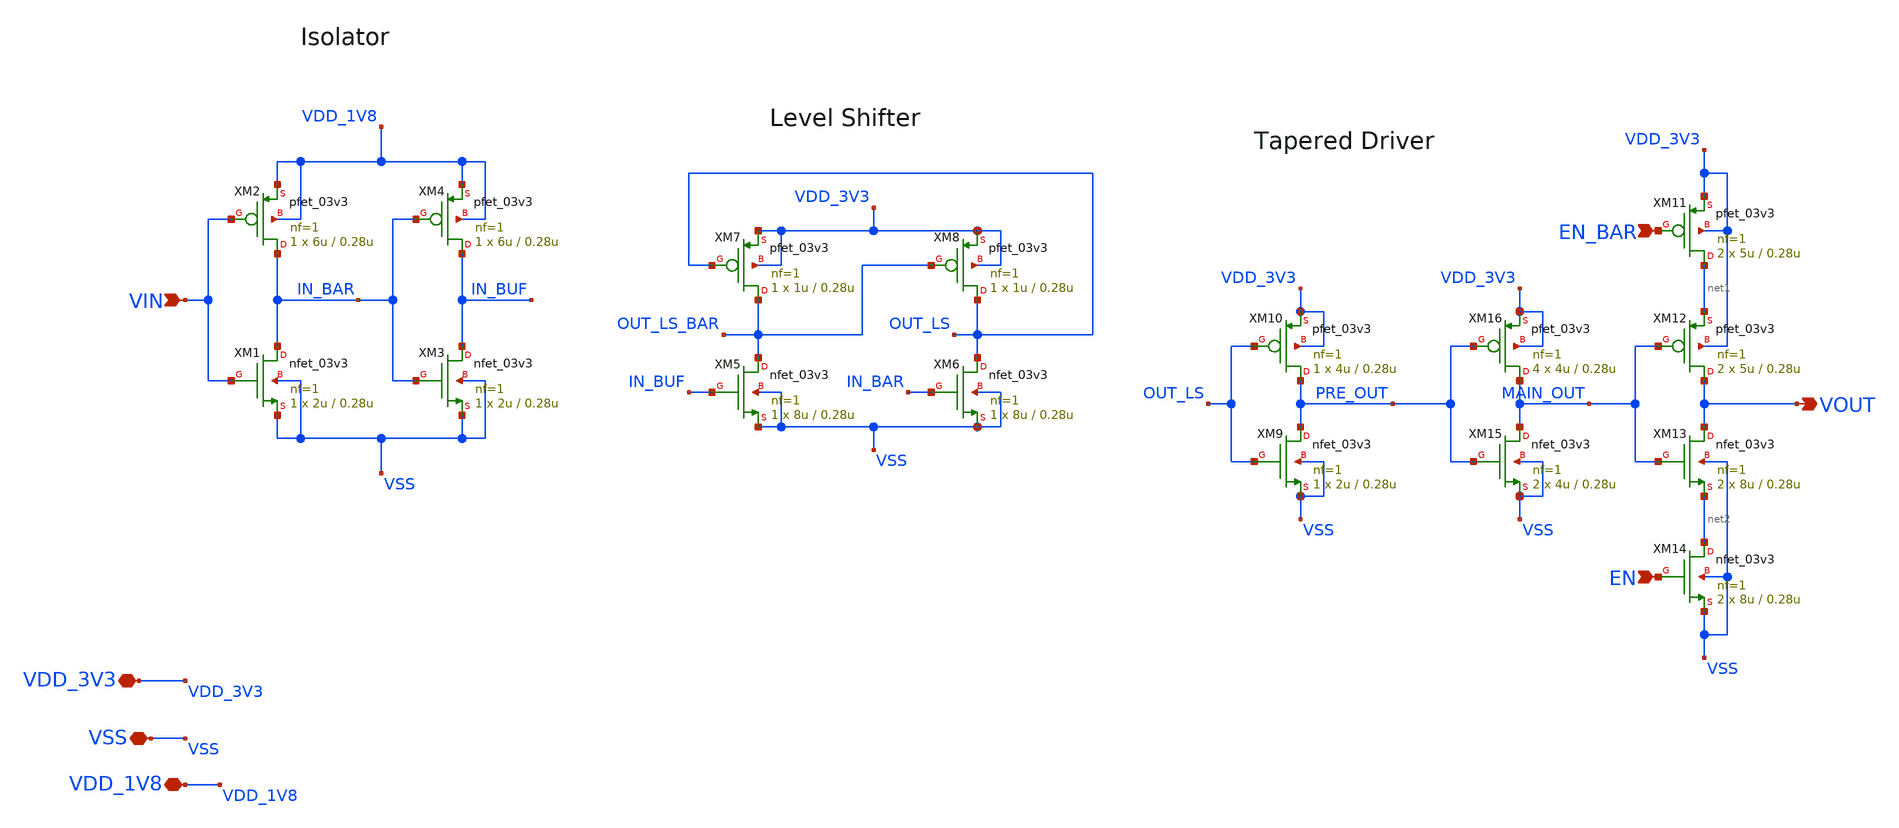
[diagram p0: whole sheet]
** sch_path: src/Output_Buffer/output_buffer.sch
**.subckt output_buffer VIN VSS VDD_1V8 EN EN_BAR VOUT VDD_3V3
*.ipin VIN
*.iopin VSS
*.iopin VDD_1V8
*.ipin EN
*.ipin EN_BAR
*.opin VOUT
*.iopin VDD_3V3
XM1 IN_BAR VIN VSS VSS nfet_03v3 L=0.28u W=2u nf=1 ad='int((nf+1)/2) * W/nf * 0.18u' as='int((nf+2)/2) * W/nf * 0.18u'
+ pd='2*int((nf+1)/2) * (W/nf + 0.18u)' ps='2*int((nf+2)/2) * (W/nf + 0.18u)' nrd='0.18u / W' nrs='0.18u / W'
+ sa=0 sb=0 sd=0 m=1
XM2 IN_BAR VIN VDD_1V8 VDD_1V8 pfet_03v3 L=0.28u W=6u nf=1 ad='int((nf+1)/2) * W/nf * 0.18u' as='int((nf+2)/2) * W/nf * 0.18u'
+ pd='2*int((nf+1)/2) * (W/nf + 0.18u)' ps='2*int((nf+2)/2) * (W/nf + 0.18u)' nrd='0.18u / W' nrs='0.18u / W'
+ sa=0 sb=0 sd=0 m=1
XM3 IN_BUF IN_BAR VSS VSS nfet_03v3 L=0.28u W=2u nf=1 ad='int((nf+1)/2) * W/nf * 0.18u' as='int((nf+2)/2) * W/nf * 0.18u'
+ pd='2*int((nf+1)/2) * (W/nf + 0.18u)' ps='2*int((nf+2)/2) * (W/nf + 0.18u)' nrd='0.18u / W' nrs='0.18u / W'
+ sa=0 sb=0 sd=0 m=1
XM4 IN_BUF IN_BAR VDD_1V8 VDD_1V8 pfet_03v3 L=0.28u W=6u nf=1 ad='int((nf+1)/2) * W/nf * 0.18u' as='int((nf+2)/2) * W/nf * 0.18u'
+ pd='2*int((nf+1)/2) * (W/nf + 0.18u)' ps='2*int((nf+2)/2) * (W/nf + 0.18u)' nrd='0.18u / W' nrs='0.18u / W'
+ sa=0 sb=0 sd=0 m=1
XM5 OUT_LS_BAR IN_BUF VSS VSS nfet_03v3 L=0.28u W=8u nf=1 ad='int((nf+1)/2) * W/nf * 0.18u' as='int((nf+2)/2) * W/nf * 0.18u'
+ pd='2*int((nf+1)/2) * (W/nf + 0.18u)' ps='2*int((nf+2)/2) * (W/nf + 0.18u)' nrd='0.18u / W' nrs='0.18u / W'
+ sa=0 sb=0 sd=0 m=1
XM6 OUT_LS IN_BAR VSS VSS nfet_03v3 L=0.28u W=8u nf=1 ad='int((nf+1)/2) * W/nf * 0.18u' as='int((nf+2)/2) * W/nf * 0.18u'
+ pd='2*int((nf+1)/2) * (W/nf + 0.18u)' ps='2*int((nf+2)/2) * (W/nf + 0.18u)' nrd='0.18u / W' nrs='0.18u / W'
+ sa=0 sb=0 sd=0 m=1
XM7 OUT_LS_BAR OUT_LS VDD_3V3 VDD_3V3 pfet_03v3 L=0.28u W=1u nf=1 ad='int((nf+1)/2) * W/nf * 0.18u' as='int((nf+2)/2) * W/nf * 0.18u'
+ pd='2*int((nf+1)/2) * (W/nf + 0.18u)' ps='2*int((nf+2)/2) * (W/nf + 0.18u)' nrd='0.18u / W' nrs='0.18u / W'
+ sa=0 sb=0 sd=0 m=1
XM8 OUT_LS OUT_LS_BAR VDD_3V3 VDD_3V3 pfet_03v3 L=0.28u W=1u nf=1 ad='int((nf+1)/2) * W/nf * 0.18u' as='int((nf+2)/2) * W/nf * 0.18u'
+ pd='2*int((nf+1)/2) * (W/nf + 0.18u)' ps='2*int((nf+2)/2) * (W/nf + 0.18u)' nrd='0.18u / W' nrs='0.18u / W'
+ sa=0 sb=0 sd=0 m=1
XM9 PRE_OUT OUT_LS VSS VSS nfet_03v3 L=0.28u W=2u nf=1 ad='int((nf+1)/2) * W/nf * 0.18u' as='int((nf+2)/2) * W/nf * 0.18u'
+ pd='2*int((nf+1)/2) * (W/nf + 0.18u)' ps='2*int((nf+2)/2) * (W/nf + 0.18u)' nrd='0.18u / W' nrs='0.18u / W'
+ sa=0 sb=0 sd=0 m=1
XM10 PRE_OUT OUT_LS VDD_3V3 VDD_3V3 pfet_03v3 L=0.28u W=4u nf=1 ad='int((nf+1)/2) * W/nf * 0.18u' as='int((nf+2)/2) * W/nf * 0.18u'
+ pd='2*int((nf+1)/2) * (W/nf + 0.18u)' ps='2*int((nf+2)/2) * (W/nf + 0.18u)' nrd='0.18u / W' nrs='0.18u / W'
+ sa=0 sb=0 sd=0 m=1
XM11 net1 EN_BAR VDD_3V3 VDD_3V3 pfet_03v3 L=0.28u W=5u nf=1 ad='int((nf+1)/2) * W/nf * 0.18u' as='int((nf+2)/2) * W/nf * 0.18u'
+ pd='2*int((nf+1)/2) * (W/nf + 0.18u)' ps='2*int((nf+2)/2) * (W/nf + 0.18u)' nrd='0.18u / W' nrs='0.18u / W'
+ sa=0 sb=0 sd=0 m=2
XM12 VOUT MAIN_OUT net1 VDD_3V3 pfet_03v3 L=0.28u W=5u nf=1 ad='int((nf+1)/2) * W/nf * 0.18u' as='int((nf+2)/2) * W/nf * 0.18u'
+ pd='2*int((nf+1)/2) * (W/nf + 0.18u)' ps='2*int((nf+2)/2) * (W/nf + 0.18u)' nrd='0.18u / W' nrs='0.18u / W'
+ sa=0 sb=0 sd=0 m=2
XM13 VOUT MAIN_OUT net2 VSS nfet_03v3 L=0.28u W=8u nf=1 ad='int((nf+1)/2) * W/nf * 0.18u' as='int((nf+2)/2) * W/nf * 0.18u'
+ pd='2*int((nf+1)/2) * (W/nf + 0.18u)' ps='2*int((nf+2)/2) * (W/nf + 0.18u)' nrd='0.18u / W' nrs='0.18u / W'
+ sa=0 sb=0 sd=0 m=2
XM14 net2 EN VSS VSS nfet_03v3 L=0.28u W=8u nf=1 ad='int((nf+1)/2) * W/nf * 0.18u' as='int((nf+2)/2) * W/nf * 0.18u'
+ pd='2*int((nf+1)/2) * (W/nf + 0.18u)' ps='2*int((nf+2)/2) * (W/nf + 0.18u)' nrd='0.18u / W' nrs='0.18u / W'
+ sa=0 sb=0 sd=0 m=2
XM15 MAIN_OUT PRE_OUT VSS VSS nfet_03v3 L=0.28u W=4u nf=1 ad='int((nf+1)/2) * W/nf * 0.18u' as='int((nf+2)/2) * W/nf * 0.18u'
+ pd='2*int((nf+1)/2) * (W/nf + 0.18u)' ps='2*int((nf+2)/2) * (W/nf + 0.18u)' nrd='0.18u / W' nrs='0.18u / W'
+ sa=0 sb=0 sd=0 m=2
XM16 MAIN_OUT PRE_OUT VDD_3V3 VDD_3V3 pfet_03v3 L=0.28u W=4u nf=1 ad='int((nf+1)/2) * W/nf * 0.18u' as='int((nf+2)/2) * W/nf * 0.18u'
+ pd='2*int((nf+1)/2) * (W/nf + 0.18u)' ps='2*int((nf+2)/2) * (W/nf + 0.18u)' nrd='0.18u / W' nrs='0.18u / W'
+ sa=0 sb=0 sd=0 m=4
**.ends
.end
